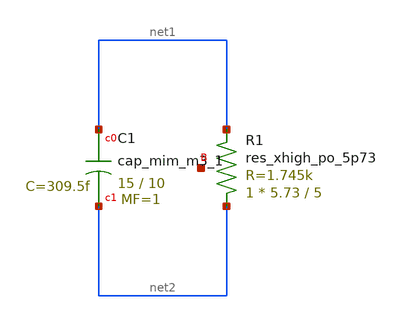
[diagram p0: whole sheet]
** sch_path: xschem/cmos_imager/photodiode_rc_model.sch
**.subckt photodiode_rc_model
XC1 net1 net2 sky130_fd_pr__cap_mim_m3_1 W=15 L=10 MF=1 m=1
XR1 net2 net1 net3 sky130_fd_pr__res_xhigh_po_5p73 L=5 mult=1 m=1
**.ends
.end
